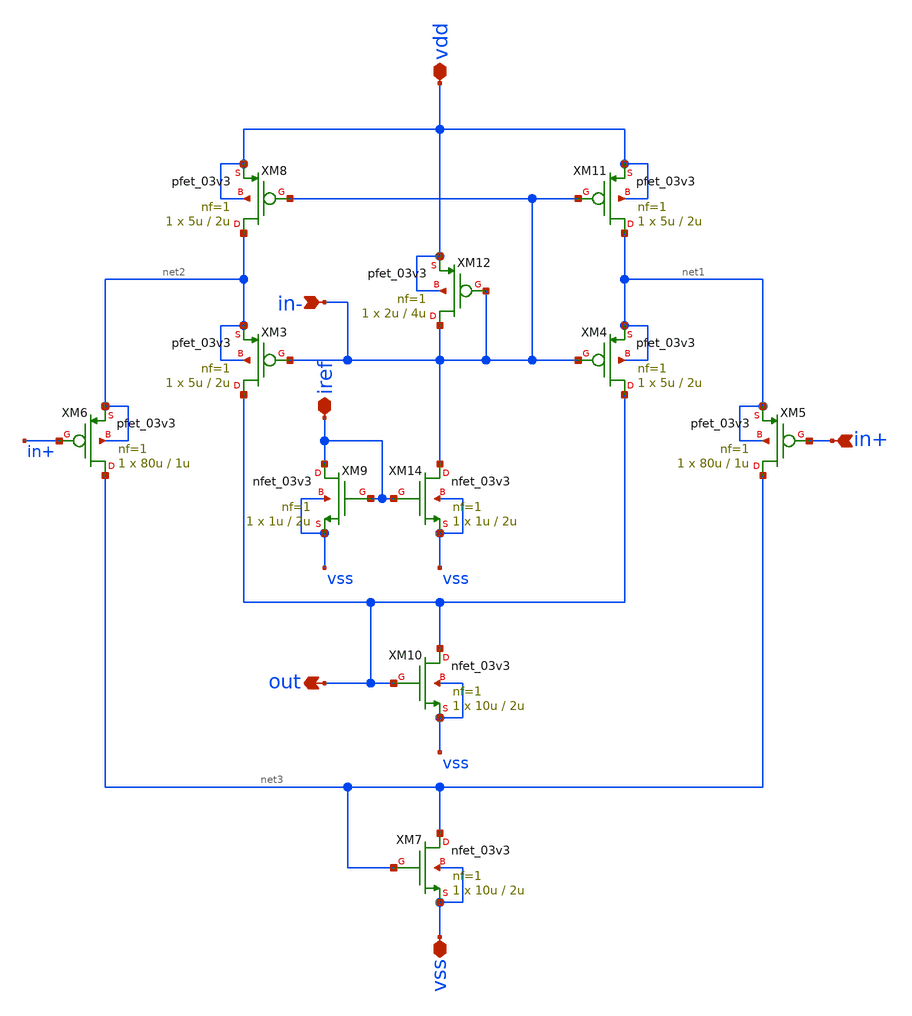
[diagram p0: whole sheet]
** sch_path: Marcel/designs/Two_Stage_CMFB_OP.sch
**.subckt Two_Stage_CMFB_OP out in- in+ vdd vss iref
*.opin out
*.ipin in-
*.ipin in+
*.iopin vdd
*.iopin vss
*.iopin iref
XM3 out in- net2 net2 pfet_03v3 L=2u W=5u nf=1 ad='int((nf+1)/2) * W/nf * 0.18u' as='int((nf+2)/2) * W/nf * 0.18u'
+ pd='2*int((nf+1)/2) * (W/nf + 0.18u)' ps='2*int((nf+2)/2) * (W/nf + 0.18u)' nrd='0.18u / W' nrs='0.18u / W'
+ sa=0 sb=0 sd=0 m=1
XM4 out in- net1 net1 pfet_03v3 L=2u W=5u nf=1 ad='int((nf+1)/2) * W/nf * 0.18u' as='int((nf+2)/2) * W/nf * 0.18u'
+ pd='2*int((nf+1)/2) * (W/nf + 0.18u)' ps='2*int((nf+2)/2) * (W/nf + 0.18u)' nrd='0.18u / W' nrs='0.18u / W'
+ sa=0 sb=0 sd=0 m=1
XM5 net3 in+ net1 net1 pfet_03v3 L=1u W=80u nf=1 ad='int((nf+1)/2) * W/nf * 0.18u' as='int((nf+2)/2) * W/nf * 0.18u'
+ pd='2*int((nf+1)/2) * (W/nf + 0.18u)' ps='2*int((nf+2)/2) * (W/nf + 0.18u)' nrd='0.18u / W' nrs='0.18u / W'
+ sa=0 sb=0 sd=0 m=1
XM6 net3 in+ net2 net2 pfet_03v3 L=1u W=80u nf=1 ad='int((nf+1)/2) * W/nf * 0.18u' as='int((nf+2)/2) * W/nf * 0.18u'
+ pd='2*int((nf+1)/2) * (W/nf + 0.18u)' ps='2*int((nf+2)/2) * (W/nf + 0.18u)' nrd='0.18u / W' nrs='0.18u / W'
+ sa=0 sb=0 sd=0 m=1
XM9 iref iref vss vss nfet_03v3 L=2u W=1u nf=1 ad='int((nf+1)/2) * W/nf * 0.18u' as='int((nf+2)/2) * W/nf * 0.18u'
+ pd='2*int((nf+1)/2) * (W/nf + 0.18u)' ps='2*int((nf+2)/2) * (W/nf + 0.18u)' nrd='0.18u / W' nrs='0.18u / W'
+ sa=0 sb=0 sd=0 m=1
XM10 out out vss vss nfet_03v3 L=2u W=10u nf=1 ad='int((nf+1)/2) * W/nf * 0.18u' as='int((nf+2)/2) * W/nf * 0.18u'
+ pd='2*int((nf+1)/2) * (W/nf + 0.18u)' ps='2*int((nf+2)/2) * (W/nf + 0.18u)' nrd='0.18u / W' nrs='0.18u / W'
+ sa=0 sb=0 sd=0 m=1
XM12 in- in- vdd vdd pfet_03v3 L=4u W=2u nf=1 ad='int((nf+1)/2) * W/nf * 0.18u' as='int((nf+2)/2) * W/nf * 0.18u'
+ pd='2*int((nf+1)/2) * (W/nf + 0.18u)' ps='2*int((nf+2)/2) * (W/nf + 0.18u)' nrd='0.18u / W' nrs='0.18u / W'
+ sa=0 sb=0 sd=0 m=1
XM14 in- iref vss vss nfet_03v3 L=2u W=1u nf=1 ad='int((nf+1)/2) * W/nf * 0.18u' as='int((nf+2)/2) * W/nf * 0.18u'
+ pd='2*int((nf+1)/2) * (W/nf + 0.18u)' ps='2*int((nf+2)/2) * (W/nf + 0.18u)' nrd='0.18u / W' nrs='0.18u / W'
+ sa=0 sb=0 sd=0 m=1
XM7 net3 net3 vss vss nfet_03v3 L=2u W=10u nf=1 ad='int((nf+1)/2) * W/nf * 0.18u' as='int((nf+2)/2) * W/nf * 0.18u'
+ pd='2*int((nf+1)/2) * (W/nf + 0.18u)' ps='2*int((nf+2)/2) * (W/nf + 0.18u)' nrd='0.18u / W' nrs='0.18u / W'
+ sa=0 sb=0 sd=0 m=1
XM8 net2 in- vdd vdd pfet_03v3 L=2u W=5u nf=1 ad='int((nf+1)/2) * W/nf * 0.18u' as='int((nf+2)/2) * W/nf * 0.18u'
+ pd='2*int((nf+1)/2) * (W/nf + 0.18u)' ps='2*int((nf+2)/2) * (W/nf + 0.18u)' nrd='0.18u / W' nrs='0.18u / W'
+ sa=0 sb=0 sd=0 m=1
XM11 net1 in- vdd vdd pfet_03v3 L=2u W=5u nf=1 ad='int((nf+1)/2) * W/nf * 0.18u' as='int((nf+2)/2) * W/nf * 0.18u'
+ pd='2*int((nf+1)/2) * (W/nf + 0.18u)' ps='2*int((nf+2)/2) * (W/nf + 0.18u)' nrd='0.18u / W' nrs='0.18u / W'
+ sa=0 sb=0 sd=0 m=1
**.ends
.end
